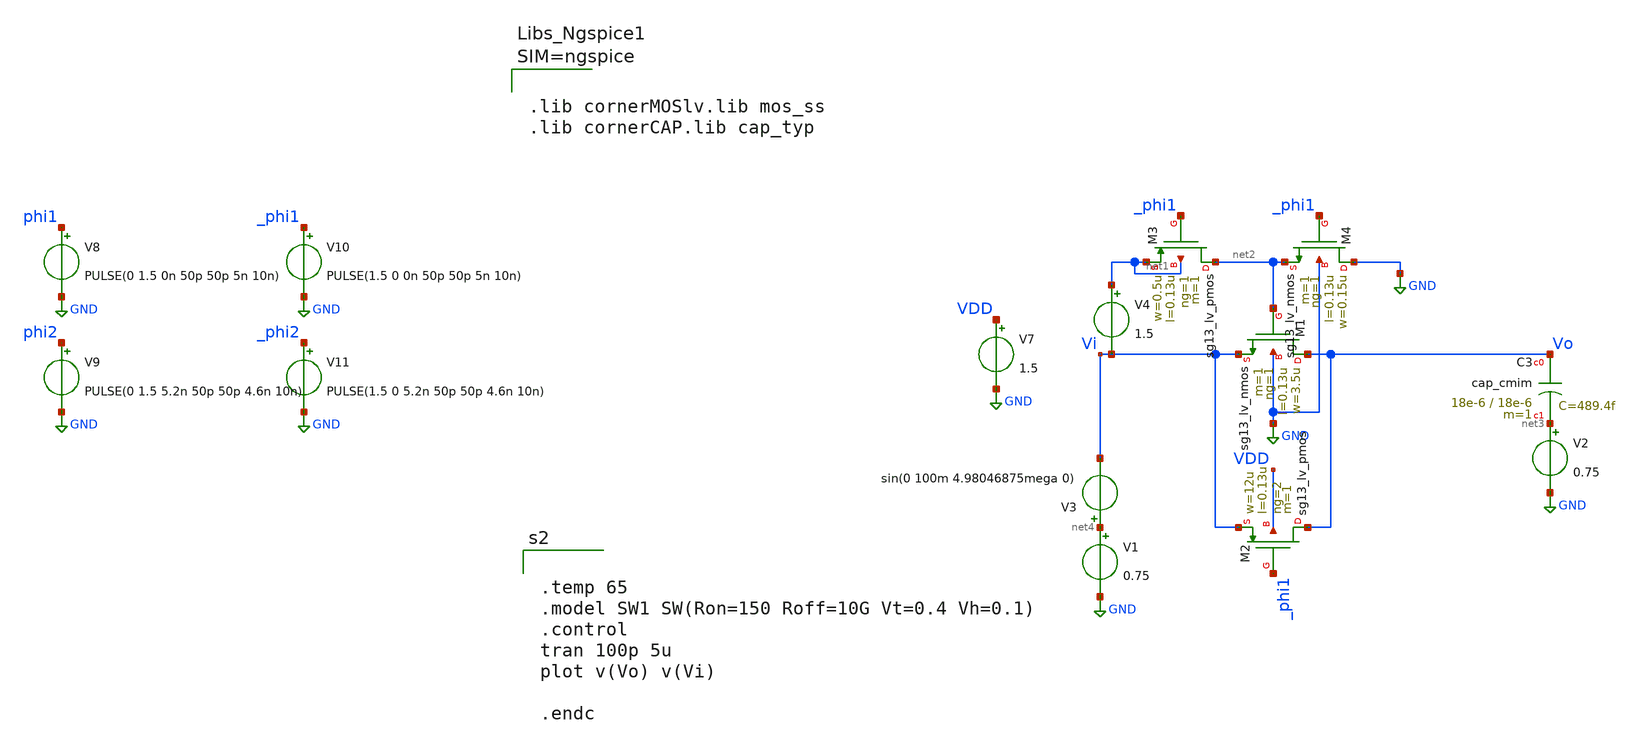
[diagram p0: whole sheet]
** sch_path: sch/tb/sw_boost.sch
**.subckt sw_boost
XC3 Vo net3 cap_cmim w=18e-6 l=18e-6 m=1 mm_ok=1
V3 net4 Vi sin(0 100m 4.98046875mega 0)
V1 net4 GND 0.75
V2 net3 GND 0.75
XM1 Vo net2 Vi GND sg13_lv_nmos w=3.5u l=0.13u ng=1 m=1 mm_ok=1
V4 net1 Vi 1.5
XM2 Vo _phi1 Vi VDD sg13_lv_pmos w=12u l=0.13u ng=2 m=1 mm_ok=1
V7 VDD GND 1.5
XM3 net2 _phi1 net1 net1 sg13_lv_pmos w=0.5u l=0.13u ng=1 m=1 mm_ok=1
XM4 GND _phi1 net2 GND sg13_lv_nmos w=0.15u l=0.13u ng=1 m=1 mm_ok=1
V8 phi1 GND PULSE(0 1.5 0n 50p 50p 5n 10n)
V9 phi2 GND PULSE(0 1.5 5.2n 50p 50p 4.6n 10n)
V10 _phi1 GND PULSE(1.5 0 0n 50p 50p 5n 10n)
V11 _phi2 GND PULSE(1.5 0 5.2n 50p 50p 4.6n 10n)
**** begin user architecture code



.lib cornerMOSlv.lib mos_ss
.lib cornerCAP.lib cap_typ





.temp 65
.model SW1 SW(Ron=150 Roff=10G Vt=0.4 Vh=0.1)
.control
tran 100p 5u
plot v(Vo) v(Vi)

.endc



**** end user architecture code
**.ends
.GLOBAL GND
.end
